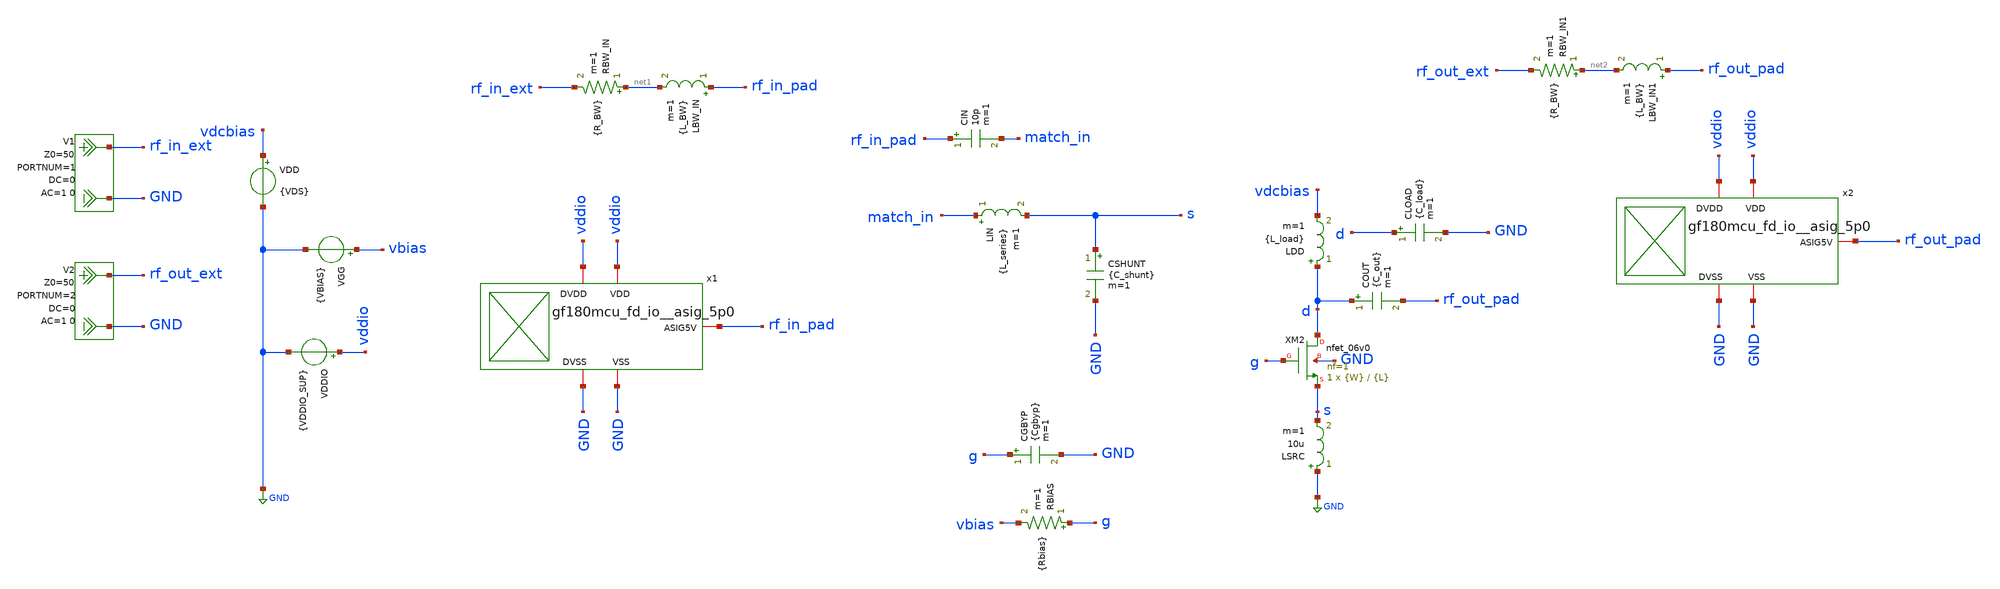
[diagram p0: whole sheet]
** sch_path: NFmin_Simulation/simulations/lna_core_06V_sweep.sch
**.subckt lna_core_06V_sweep
VGG vbias GND {VBIAS}
VDD vdcbias GND {VDS}
LDD d vdcbias {L_load} m=1
COUT d rf_out_pad {C_out} m=1
CIN rf_in_pad match_in 10p m=1
V1 rf_in_ext GND DC 0 AC 1 0 portnum 1 z0 50
V2 rf_out_ext GND DC 0 AC 1 0 portnum 2 z0 50
LSRC GND s 10u m=1
XM2 d g s GND nfet_06v0 L={L} W={W} nf=1 ad='int((nf+1)/2) * W/nf * 0.18u' as='int((nf+2)/2) * W/nf * 0.18u'
+ pd='2*int((nf+1)/2) * (W/nf + 0.18u)' ps='2*int((nf+2)/2) * (W/nf + 0.18u)' nrd='0.18u / W' nrs='0.18u / W'
+ sa=0 sb=0 sd=0 m=1
LIN match_in s {L_series} m=1
CSHUNT s GND {C_shunt} m=1
RBIAS g vbias {Rbias} m=1
CGBYP g GND {Cgbyp} m=1
CLOAD d GND {C_load} m=1
x1 rf_in_pad vddio GND vddio GND gf180mcu_fd_io__asig_5p0
LBW_IN rf_in_pad net1 {L_BW} m=1
RBW_IN net1 rf_in_ext {R_BW} m=1
VDDIO vddio GND {VDDIO_SUP}
x2 rf_out_pad vddio GND vddio GND gf180mcu_fd_io__asig_5p0
LBW_IN1 rf_out_pad net2 {L_BW} m=1
RBW_IN1 net2 rf_out_ext {R_BW} m=1
**** begin user architecture code

.include /foss/pdks/gf180mcuD/libs.tech/ngspice/design.ngspice

.lib /foss/pdks/gf180mcuD/libs.tech/ngspice/sm141064.ngspice typical
.lib /foss/pdks/gf180mcuD/libs.tech/ngspice/sm141064.ngspice res_typical
.lib /foss/pdks/gf180mcuD/libs.tech/ngspice/sm141064.ngspice moscap_typical
.lib /foss/pdks/gf180mcuD/libs.tech/ngspice/sm141064.ngspice diode_typical

*.include /foss/pdks/gf180mcuD/libs.ref/gf180mcu_fd_io/spice/gf180mcu_fd_io.spice
.include /media/sf_LNA_chipathon/The-Silent-Owl-GF180MCU-WB-LNA/analog_pad_sp_paramerters/xschem/gf180mcu_fd_io__asig_5p0.spice



* ============================================================
* 6 V common-gate LNA
* Best fixed point after W/VBIAS/passive retune
*
* Assumes model .include/.lib lines are already elsewhere.
* ============================================================
.param VBIAS=1.80
.param VDS=5.0

.param VDDIO_SUP=5.0
.param L_BW=1n
.param R_BW=0.2

.param W=80e-6
.param L=0.60e-6

.param L_series=4.8n
.param C_shunt=0.50p

.param L_load=4.0n
.param C_load=0.85p
.param C_out=0.20p

.param Rbias=50k
.param Cgbyp=20p

.option savecurrents

.param fnoicor=0
.param sw_stat_mismatch=0

.control
  set noaskquit
  set wr_singlescale
  set wr_vecnames

  echo ============================================================
  echo 6 V CG LNA final fixed-point verification
  echo VBIAS=1.80 V, W=80 um, L=0.60 um
  echo ============================================================

  op

  let id_op = abs(i(vdd))
  let gm_op = @m.xm2.m0[gm]
  let gds_op = @m.xm2.m0[gds]

  let vgs_op = v(g)-v(s)
  let vds_op = v(d)-v(s)
  let vbs_op = -v(s)

  let pdc_op = 1e3*id_op*vds_op
  let gm_id_op = gm_op/id_op
  let ro_op = 1/gds_op
  let gmro_op = gm_op/gds_op
  let rin_cg_op = 1/gm_op

  set id_s = $&id_op
  set gm_s = $&gm_op
  set gds_s = $&gds_op
  set vgs_s = $&vgs_op
  set vds_s = $&vds_op
  set vbs_s = $&vbs_op
  set pdc_s = $&pdc_op
  set gm_id_s = $&gm_id_op
  set ro_s = $&ro_op
  set gmro_s = $&gmro_op
  set rin_s = $&rin_cg_op

  echo Operating point:
  print v(g) v(s) v(d)
  print vgs_op vds_op vbs_op
  print id_op pdc_op
  print gm_op gds_op gm_id_op ro_op gmro_op rin_cg_op

  destroy $curplot

  echo ============================================================
  echo Exact 2.4 GHz point
  echo ============================================================

  echo VBIAS_V W_m L_m L_series_H C_shunt_F L_load_H C_load_F C_out_F VGS_V VDS_V VBS_V ID_A Pdc_mW
+ gm_S gds_S gm_ID_1_per_V ro_Ohm gmro Rin_CG_Ohm S11_dB S21_dB S12_dB S22_dB NF_dB NFmin_dB K_stab >
+ lna06_cg_final_2p4GHz_point.txt

  sp lin 1 2.4e9 2.4e9 1

  let s11_db = db(s_1_1)
  let s21_db = db(s_2_1)
  let s12_db = db(s_1_2)
  let s22_db = db(s_2_2)

  let nf_db = real(NF)
  let nfmin_db = real(NFmin)

  let mag_s11 = mag(s_1_1)
  let mag_s12 = mag(s_1_2)
  let mag_s21 = mag(s_2_1)
  let mag_s22 = mag(s_2_2)

  let delta = s_1_1*s_2_2 - s_1_2*s_2_1
  let mag_delta = mag(delta)

  let k_stab = (1 - mag_s11*mag_s11 - mag_s22*mag_s22 + mag_delta*mag_delta)/(2*mag_s12*mag_s21)

  print s11_db s21_db s12_db s22_db
  print nf_db nfmin_db k_stab

  let vbias_save = 1.80
  let w_save = 80e-6
  let l_save = 0.60e-6
  let lseries_save = 4.8e-9
  let cshunt_save = 0.50e-12
  let lload_save = 4.0e-9
  let cload_save = 0.85e-12
  let cout_save = 0.20e-12

  echo $&vbias_save $&w_save $&l_save $&lseries_save $&cshunt_save $&lload_save $&cload_save
+ $&cout_save $vgs_s $vds_s $vbs_s $id_s $pdc_s $gm_s $gds_s $gm_id_s $ro_s $gmro_s $rin_s $&s11_db $&s21_db
+ $&s12_db $&s22_db $&nf_db $&nfmin_db $&k_stab >> lna06_cg_final_2p4GHz_point.txt

  destroy $curplot

  echo ============================================================
  echo Broadband sweep: 100 MHz to 20 GHz
  echo ============================================================

  sp dec 101 100Meg 20Gig 1

  let s11_db = db(s_1_1)
  let s21_db = db(s_2_1)
  let s12_db = db(s_1_2)
  let s22_db = db(s_2_2)

  let nf_db = real(NF)
  let nfmin_db = real(NFmin)

  let mag_s11 = mag(s_1_1)
  let mag_s12 = mag(s_1_2)
  let mag_s21 = mag(s_2_1)
  let mag_s22 = mag(s_2_2)

  let delta = s_1_1*s_2_2 - s_1_2*s_2_1
  let mag_delta = mag(delta)

  let k_stab = (1 - mag_s11*mag_s11 - mag_s22*mag_s22 + mag_delta*mag_delta)/(2*mag_s12*mag_s21)

  wrdata lna06_cg_final_broadband.txt s11_db s21_db s12_db s22_db nf_db nfmin_db k_stab

  echo ============================================================
  echo Done.
  echo Files generated:
  echo   lna06_cg_final_2p4GHz_point.txt
  echo   lna06_cg_final_broadband.txt
  echo ============================================================

.endc


**** end user architecture code
**.ends
.GLOBAL GND
.end
